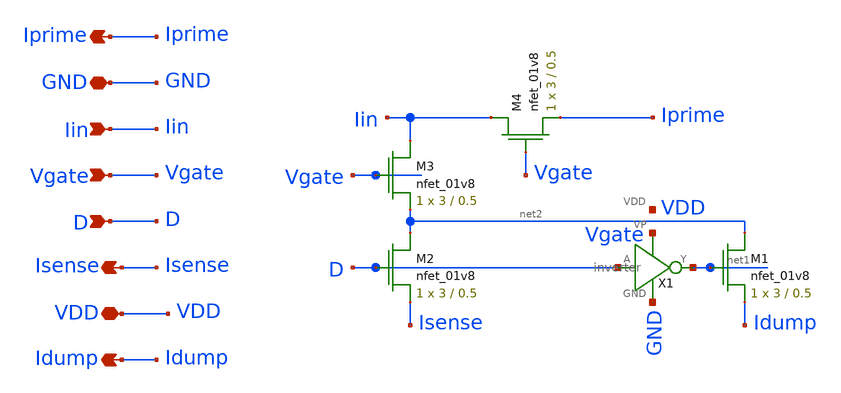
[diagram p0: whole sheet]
** sch_path: final/LDS/daccell_LDS.sch
**.subckt daccell_LDS GND Isense Idump Iin Iprime Vgate D VDD
*.iopin GND
*.opin Isense
*.opin Idump
*.ipin Iin
*.opin Iprime
*.ipin Vgate
*.ipin D
*.iopin VDD
XM2 net2 D Isense GND sky130_fd_pr__nfet_01v8 L=0.5 W=3 nf=1 ad='int((nf+1)/2) * W/nf * 0.29' as='int((nf+2)/2) * W/nf * 0.29'
+ pd='2*int((nf+1)/2) * (W/nf + 0.29)' ps='2*int((nf+2)/2) * (W/nf + 0.29)' nrd='0.29 / W' nrs='0.29 / W'
+ sa=0 sb=0 sd=0 mult=1 m=1
X1 Vgate D net1 GND VDD inverter
XM1 net2 net1 Idump GND sky130_fd_pr__nfet_01v8 L=0.5 W=3 nf=1 ad='int((nf+1)/2) * W/nf * 0.29' as='int((nf+2)/2) * W/nf * 0.29'
+ pd='2*int((nf+1)/2) * (W/nf + 0.29)' ps='2*int((nf+2)/2) * (W/nf + 0.29)' nrd='0.29 / W' nrs='0.29 / W'
+ sa=0 sb=0 sd=0 mult=1 m=1
XM3 Iin Vgate net2 GND sky130_fd_pr__nfet_01v8 L=0.5 W=3 nf=1 ad='int((nf+1)/2) * W/nf * 0.29' as='int((nf+2)/2) * W/nf * 0.29'
+ pd='2*int((nf+1)/2) * (W/nf + 0.29)' ps='2*int((nf+2)/2) * (W/nf + 0.29)' nrd='0.29 / W' nrs='0.29 / W'
+ sa=0 sb=0 sd=0 mult=1 m=1
XM4 Iin Vgate Iprime GND sky130_fd_pr__nfet_01v8 L=0.5 W=3 nf=1 ad='int((nf+1)/2) * W/nf * 0.29' as='int((nf+2)/2) * W/nf * 0.29'
+ pd='2*int((nf+1)/2) * (W/nf + 0.29)' ps='2*int((nf+2)/2) * (W/nf + 0.29)' nrd='0.29 / W' nrs='0.29 / W'
+ sa=0 sb=0 sd=0 mult=1 m=1
**.ends

* expanding   symbol:  inverter.sym # of pins=5
** sym_path: final/LDS/inverter.sym
** sch_path: final/LDS/inverter.sch
.subckt inverter VP A Y GND VDD
*.ipin A
*.iopin VP
*.iopin GND
*.opin Y
*.iopin VDD
XM1 Y A VP VDD sky130_fd_pr__pfet_01v8 L=0.5 W=3 nf=1 ad='int((nf+1)/2) * W/nf * 0.29' as='int((nf+2)/2) * W/nf * 0.29'
+ pd='2*int((nf+1)/2) * (W/nf + 0.29)' ps='2*int((nf+2)/2) * (W/nf + 0.29)' nrd='0.29 / W' nrs='0.29 / W'
+ sa=0 sb=0 sd=0 mult=1 m=1
XM2 Y A GND GND sky130_fd_pr__nfet_01v8 L=0.5 W=3 nf=1 ad='int((nf+1)/2) * W/nf * 0.29' as='int((nf+2)/2) * W/nf * 0.29'
+ pd='2*int((nf+1)/2) * (W/nf + 0.29)' ps='2*int((nf+2)/2) * (W/nf + 0.29)' nrd='0.29 / W' nrs='0.29 / W'
+ sa=0 sb=0 sd=0 mult=1 m=1
.ends

.end
